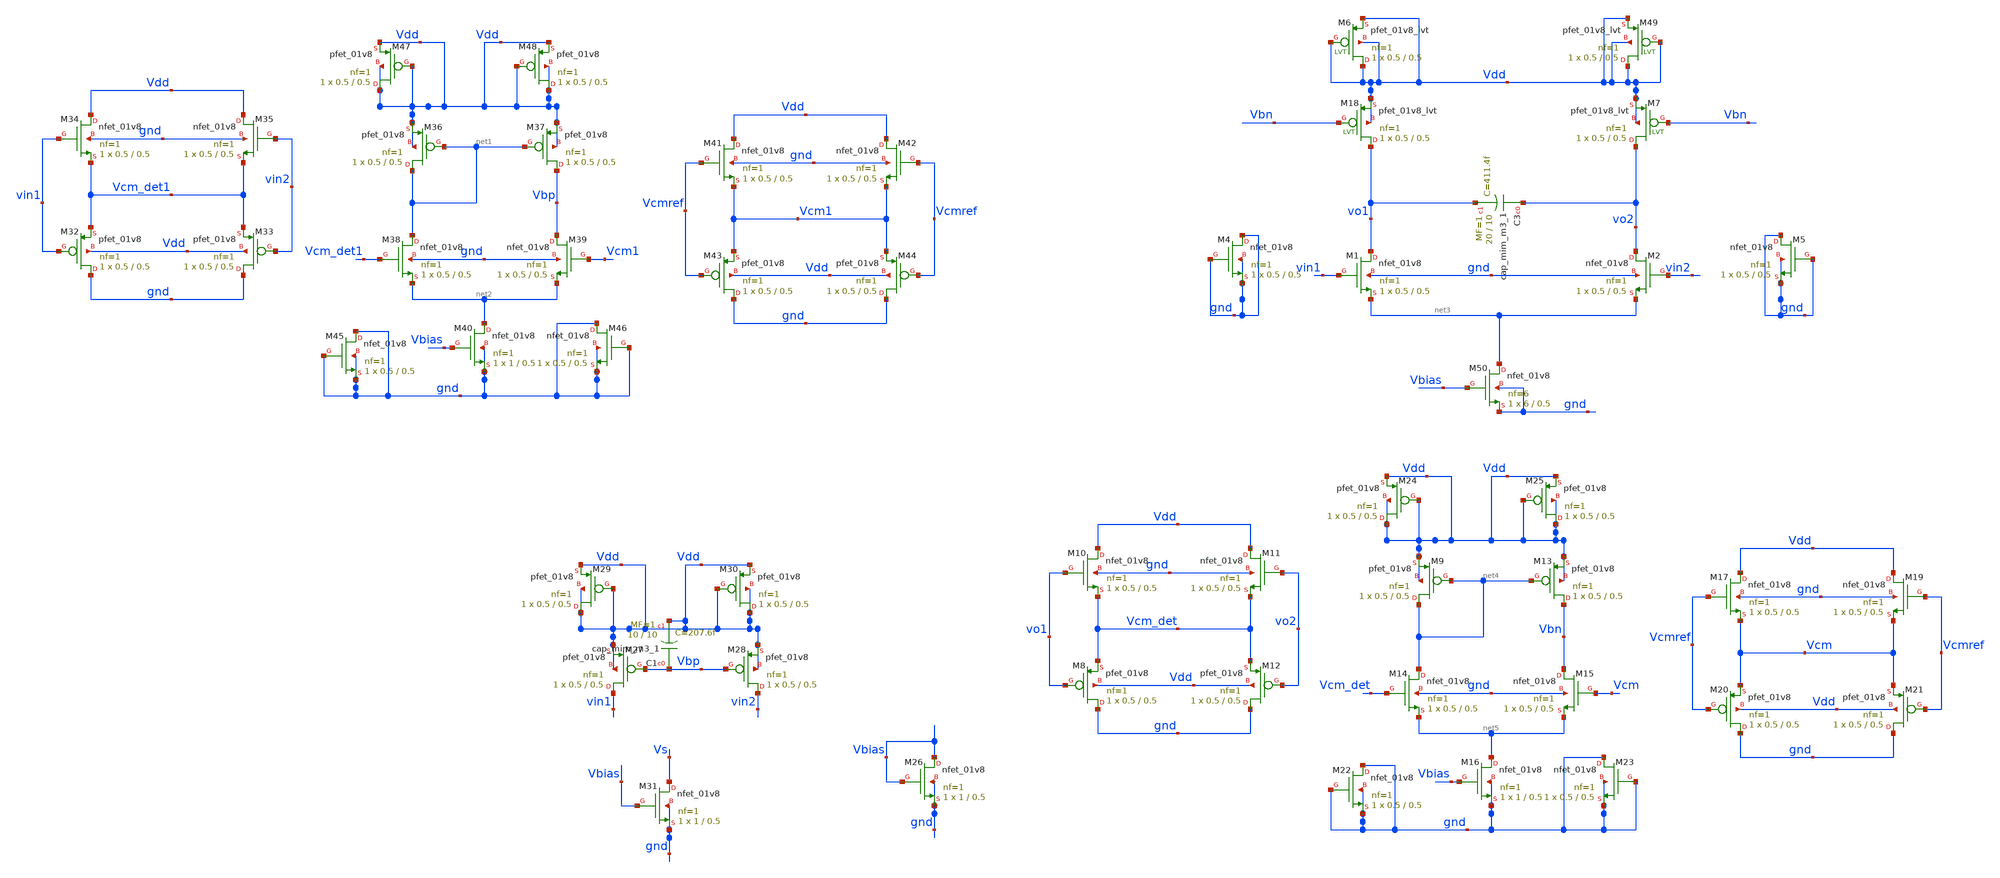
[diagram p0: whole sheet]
** sch_path: xschem/xschemfiles/full_new1.sch
**.subckt full_new1
XM26 Vbias Vbias gnd gnd sky130_fd_pr__nfet_01v8 L=0.5 W=1 nf=1 ad='int((nf+1)/2) * W/nf * 0.29' as='int((nf+2)/2) * W/nf * 0.29'
+ pd='2*int((nf+1)/2) * (W/nf + 0.29)' ps='2*int((nf+2)/2) * (W/nf + 0.29)' nrd='0.29 / W' nrs='0.29 / W'
+ sa=0 sb=0 sd=0 mult=1 m=1
XM27 vin1 Vbp Vdd Vdd sky130_fd_pr__pfet_01v8 L=0.5 W=0.5 nf=1 ad='int((nf+1)/2) * W/nf * 0.29' as='int((nf+2)/2) * W/nf * 0.29'
+ pd='2*int((nf+1)/2) * (W/nf + 0.29)' ps='2*int((nf+2)/2) * (W/nf + 0.29)' nrd='0.29 / W' nrs='0.29 / W'
+ sa=0 sb=0 sd=0 mult=1 m=1
XM28 vin2 Vbp Vdd Vdd sky130_fd_pr__pfet_01v8 L=0.5 W=0.5 nf=1 ad='int((nf+1)/2) * W/nf * 0.29' as='int((nf+2)/2) * W/nf * 0.29'
+ pd='2*int((nf+1)/2) * (W/nf + 0.29)' ps='2*int((nf+2)/2) * (W/nf + 0.29)' nrd='0.29 / W' nrs='0.29 / W'
+ sa=0 sb=0 sd=0 mult=1 m=1
XM29 Vdd Vdd Vdd Vdd sky130_fd_pr__pfet_01v8 L=0.5 W=0.5 nf=1 ad='int((nf+1)/2) * W/nf * 0.29' as='int((nf+2)/2) * W/nf * 0.29'
+ pd='2*int((nf+1)/2) * (W/nf + 0.29)' ps='2*int((nf+2)/2) * (W/nf + 0.29)' nrd='0.29 / W' nrs='0.29 / W'
+ sa=0 sb=0 sd=0 mult=1 m=1
XM30 Vdd Vdd Vdd Vdd sky130_fd_pr__pfet_01v8 L=0.5 W=0.5 nf=1 ad='int((nf+1)/2) * W/nf * 0.29' as='int((nf+2)/2) * W/nf * 0.29'
+ pd='2*int((nf+1)/2) * (W/nf + 0.29)' ps='2*int((nf+2)/2) * (W/nf + 0.29)' nrd='0.29 / W' nrs='0.29 / W'
+ sa=0 sb=0 sd=0 mult=1 m=1
XM31 Vs Vbias gnd gnd sky130_fd_pr__nfet_01v8 L=0.5 W=1 nf=1 ad='int((nf+1)/2) * W/nf * 0.29' as='int((nf+2)/2) * W/nf * 0.29'
+ pd='2*int((nf+1)/2) * (W/nf + 0.29)' ps='2*int((nf+2)/2) * (W/nf + 0.29)' nrd='0.29 / W' nrs='0.29 / W'
+ sa=0 sb=0 sd=0 mult=1 m=1
XC1 Vbp Vdd sky130_fd_pr__cap_mim_m3_1 W=10 L=10 MF=1 m=1
XM32 gnd vin1 Vcm_det1 Vdd sky130_fd_pr__pfet_01v8 L=0.5 W=0.5 nf=1 ad='int((nf+1)/2) * W/nf * 0.29'
+ as='int((nf+2)/2) * W/nf * 0.29' pd='2*int((nf+1)/2) * (W/nf + 0.29)' ps='2*int((nf+2)/2) * (W/nf + 0.29)'
+ nrd='0.29 / W' nrs='0.29 / W' sa=0 sb=0 sd=0 mult=1 m=1
XM33 gnd vin2 Vcm_det1 Vdd sky130_fd_pr__pfet_01v8 L=0.5 W=0.5 nf=1 ad='int((nf+1)/2) * W/nf * 0.29'
+ as='int((nf+2)/2) * W/nf * 0.29' pd='2*int((nf+1)/2) * (W/nf + 0.29)' ps='2*int((nf+2)/2) * (W/nf + 0.29)'
+ nrd='0.29 / W' nrs='0.29 / W' sa=0 sb=0 sd=0 mult=1 m=1
XM34 Vdd vin1 Vcm_det1 gnd sky130_fd_pr__nfet_01v8 L=0.5 W=0.5 nf=1 ad='int((nf+1)/2) * W/nf * 0.29'
+ as='int((nf+2)/2) * W/nf * 0.29' pd='2*int((nf+1)/2) * (W/nf + 0.29)' ps='2*int((nf+2)/2) * (W/nf + 0.29)'
+ nrd='0.29 / W' nrs='0.29 / W' sa=0 sb=0 sd=0 mult=1 m=1
XM35 Vdd vin2 Vcm_det1 gnd sky130_fd_pr__nfet_01v8 L=0.5 W=0.5 nf=1 ad='int((nf+1)/2) * W/nf * 0.29'
+ as='int((nf+2)/2) * W/nf * 0.29' pd='2*int((nf+1)/2) * (W/nf + 0.29)' ps='2*int((nf+2)/2) * (W/nf + 0.29)'
+ nrd='0.29 / W' nrs='0.29 / W' sa=0 sb=0 sd=0 mult=1 m=1
XM36 net1 net1 Vdd Vdd sky130_fd_pr__pfet_01v8 L=0.5 W=0.5 nf=1 ad='int((nf+1)/2) * W/nf * 0.29' as='int((nf+2)/2) * W/nf * 0.29'
+ pd='2*int((nf+1)/2) * (W/nf + 0.29)' ps='2*int((nf+2)/2) * (W/nf + 0.29)' nrd='0.29 / W' nrs='0.29 / W'
+ sa=0 sb=0 sd=0 mult=1 m=1
XM37 Vbp net1 Vdd Vdd sky130_fd_pr__pfet_01v8 L=0.5 W=0.5 nf=1 ad='int((nf+1)/2) * W/nf * 0.29' as='int((nf+2)/2) * W/nf * 0.29'
+ pd='2*int((nf+1)/2) * (W/nf + 0.29)' ps='2*int((nf+2)/2) * (W/nf + 0.29)' nrd='0.29 / W' nrs='0.29 / W'
+ sa=0 sb=0 sd=0 mult=1 m=1
XM38 net1 Vcm_det1 net2 gnd sky130_fd_pr__nfet_01v8 L=0.5 W=0.5 nf=1 ad='int((nf+1)/2) * W/nf * 0.29'
+ as='int((nf+2)/2) * W/nf * 0.29' pd='2*int((nf+1)/2) * (W/nf + 0.29)' ps='2*int((nf+2)/2) * (W/nf + 0.29)'
+ nrd='0.29 / W' nrs='0.29 / W' sa=0 sb=0 sd=0 mult=1 m=1
XM39 Vbp Vcm1 net2 gnd sky130_fd_pr__nfet_01v8 L=0.5 W=0.5 nf=1 ad='int((nf+1)/2) * W/nf * 0.29' as='int((nf+2)/2) * W/nf * 0.29'
+ pd='2*int((nf+1)/2) * (W/nf + 0.29)' ps='2*int((nf+2)/2) * (W/nf + 0.29)' nrd='0.29 / W' nrs='0.29 / W'
+ sa=0 sb=0 sd=0 mult=1 m=1
XM40 net2 Vbias gnd gnd sky130_fd_pr__nfet_01v8 L=0.5 W=1 nf=1 ad='int((nf+1)/2) * W/nf * 0.29' as='int((nf+2)/2) * W/nf * 0.29'
+ pd='2*int((nf+1)/2) * (W/nf + 0.29)' ps='2*int((nf+2)/2) * (W/nf + 0.29)' nrd='0.29 / W' nrs='0.29 / W'
+ sa=0 sb=0 sd=0 mult=1 m=1
XM41 Vdd Vcmref Vcm1 gnd sky130_fd_pr__nfet_01v8 L=0.5 W=0.5 nf=1 ad='int((nf+1)/2) * W/nf * 0.29' as='int((nf+2)/2) * W/nf * 0.29'
+ pd='2*int((nf+1)/2) * (W/nf + 0.29)' ps='2*int((nf+2)/2) * (W/nf + 0.29)' nrd='0.29 / W' nrs='0.29 / W'
+ sa=0 sb=0 sd=0 mult=1 m=1
XM42 Vdd Vcmref Vcm1 gnd sky130_fd_pr__nfet_01v8 L=0.5 W=0.5 nf=1 ad='int((nf+1)/2) * W/nf * 0.29' as='int((nf+2)/2) * W/nf * 0.29'
+ pd='2*int((nf+1)/2) * (W/nf + 0.29)' ps='2*int((nf+2)/2) * (W/nf + 0.29)' nrd='0.29 / W' nrs='0.29 / W'
+ sa=0 sb=0 sd=0 mult=1 m=1
XM43 gnd Vcmref Vcm1 Vdd sky130_fd_pr__pfet_01v8 L=0.5 W=0.5 nf=1 ad='int((nf+1)/2) * W/nf * 0.29' as='int((nf+2)/2) * W/nf * 0.29'
+ pd='2*int((nf+1)/2) * (W/nf + 0.29)' ps='2*int((nf+2)/2) * (W/nf + 0.29)' nrd='0.29 / W' nrs='0.29 / W'
+ sa=0 sb=0 sd=0 mult=1 m=1
XM44 gnd Vcmref Vcm1 Vdd sky130_fd_pr__pfet_01v8 L=0.5 W=0.5 nf=1 ad='int((nf+1)/2) * W/nf * 0.29' as='int((nf+2)/2) * W/nf * 0.29'
+ pd='2*int((nf+1)/2) * (W/nf + 0.29)' ps='2*int((nf+2)/2) * (W/nf + 0.29)' nrd='0.29 / W' nrs='0.29 / W'
+ sa=0 sb=0 sd=0 mult=1 m=1
XM45 gnd gnd gnd gnd sky130_fd_pr__nfet_01v8 L=0.5 W=0.5 nf=1 ad='int((nf+1)/2) * W/nf * 0.29' as='int((nf+2)/2) * W/nf * 0.29'
+ pd='2*int((nf+1)/2) * (W/nf + 0.29)' ps='2*int((nf+2)/2) * (W/nf + 0.29)' nrd='0.29 / W' nrs='0.29 / W'
+ sa=0 sb=0 sd=0 mult=1 m=1
XM46 gnd gnd gnd gnd sky130_fd_pr__nfet_01v8 L=0.5 W=0.5 nf=1 ad='int((nf+1)/2) * W/nf * 0.29' as='int((nf+2)/2) * W/nf * 0.29'
+ pd='2*int((nf+1)/2) * (W/nf + 0.29)' ps='2*int((nf+2)/2) * (W/nf + 0.29)' nrd='0.29 / W' nrs='0.29 / W'
+ sa=0 sb=0 sd=0 mult=1 m=1
XM47 Vdd Vdd Vdd Vdd sky130_fd_pr__pfet_01v8 L=0.5 W=0.5 nf=1 ad='int((nf+1)/2) * W/nf * 0.29' as='int((nf+2)/2) * W/nf * 0.29'
+ pd='2*int((nf+1)/2) * (W/nf + 0.29)' ps='2*int((nf+2)/2) * (W/nf + 0.29)' nrd='0.29 / W' nrs='0.29 / W'
+ sa=0 sb=0 sd=0 mult=1 m=1
XM48 Vdd Vdd Vdd Vdd sky130_fd_pr__pfet_01v8 L=0.5 W=0.5 nf=1 ad='int((nf+1)/2) * W/nf * 0.29' as='int((nf+2)/2) * W/nf * 0.29'
+ pd='2*int((nf+1)/2) * (W/nf + 0.29)' ps='2*int((nf+2)/2) * (W/nf + 0.29)' nrd='0.29 / W' nrs='0.29 / W'
+ sa=0 sb=0 sd=0 mult=1 m=1
XM1 vo1 vin1 net3 gnd sky130_fd_pr__nfet_01v8 L=0.5 W=0.5 nf=1 ad='int((nf+1)/2) * W/nf * 0.29' as='int((nf+2)/2) * W/nf * 0.29'
+ pd='2*int((nf+1)/2) * (W/nf + 0.29)' ps='2*int((nf+2)/2) * (W/nf + 0.29)' nrd='0.29 / W' nrs='0.29 / W'
+ sa=0 sb=0 sd=0 mult=1 m=1
XM2 vo2 vin2 net3 gnd sky130_fd_pr__nfet_01v8 L=0.5 W=0.5 nf=1 ad='int((nf+1)/2) * W/nf * 0.29' as='int((nf+2)/2) * W/nf * 0.29'
+ pd='2*int((nf+1)/2) * (W/nf + 0.29)' ps='2*int((nf+2)/2) * (W/nf + 0.29)' nrd='0.29 / W' nrs='0.29 / W'
+ sa=0 sb=0 sd=0 mult=1 m=1
XC3 vo2 vo1 sky130_fd_pr__cap_mim_m3_1 W=20 L=10 MF=1 m=1
XM4 gnd gnd gnd gnd sky130_fd_pr__nfet_01v8 L=0.5 W=0.5 nf=1 ad='int((nf+1)/2) * W/nf * 0.29' as='int((nf+2)/2) * W/nf * 0.29'
+ pd='2*int((nf+1)/2) * (W/nf + 0.29)' ps='2*int((nf+2)/2) * (W/nf + 0.29)' nrd='0.29 / W' nrs='0.29 / W'
+ sa=0 sb=0 sd=0 mult=1 m=1
XM5 gnd gnd gnd gnd sky130_fd_pr__nfet_01v8 L=0.5 W=0.5 nf=1 ad='int((nf+1)/2) * W/nf * 0.29' as='int((nf+2)/2) * W/nf * 0.29'
+ pd='2*int((nf+1)/2) * (W/nf + 0.29)' ps='2*int((nf+2)/2) * (W/nf + 0.29)' nrd='0.29 / W' nrs='0.29 / W'
+ sa=0 sb=0 sd=0 mult=1 m=1
XM8 gnd vo1 Vcm_det Vdd sky130_fd_pr__pfet_01v8 L=0.5 W=0.5 nf=1 ad='int((nf+1)/2) * W/nf * 0.29' as='int((nf+2)/2) * W/nf * 0.29'
+ pd='2*int((nf+1)/2) * (W/nf + 0.29)' ps='2*int((nf+2)/2) * (W/nf + 0.29)' nrd='0.29 / W' nrs='0.29 / W'
+ sa=0 sb=0 sd=0 mult=1 m=1
XM12 gnd vo2 Vcm_det Vdd sky130_fd_pr__pfet_01v8 L=0.5 W=0.5 nf=1 ad='int((nf+1)/2) * W/nf * 0.29' as='int((nf+2)/2) * W/nf * 0.29'
+ pd='2*int((nf+1)/2) * (W/nf + 0.29)' ps='2*int((nf+2)/2) * (W/nf + 0.29)' nrd='0.29 / W' nrs='0.29 / W'
+ sa=0 sb=0 sd=0 mult=1 m=1
XM10 Vdd vo1 Vcm_det gnd sky130_fd_pr__nfet_01v8 L=0.5 W=0.5 nf=1 ad='int((nf+1)/2) * W/nf * 0.29' as='int((nf+2)/2) * W/nf * 0.29'
+ pd='2*int((nf+1)/2) * (W/nf + 0.29)' ps='2*int((nf+2)/2) * (W/nf + 0.29)' nrd='0.29 / W' nrs='0.29 / W'
+ sa=0 sb=0 sd=0 mult=1 m=1
XM11 Vdd vo2 Vcm_det gnd sky130_fd_pr__nfet_01v8 L=0.5 W=0.5 nf=1 ad='int((nf+1)/2) * W/nf * 0.29' as='int((nf+2)/2) * W/nf * 0.29'
+ pd='2*int((nf+1)/2) * (W/nf + 0.29)' ps='2*int((nf+2)/2) * (W/nf + 0.29)' nrd='0.29 / W' nrs='0.29 / W'
+ sa=0 sb=0 sd=0 mult=1 m=1
XM9 net4 net4 Vdd Vdd sky130_fd_pr__pfet_01v8 L=0.5 W=0.5 nf=1 ad='int((nf+1)/2) * W/nf * 0.29' as='int((nf+2)/2) * W/nf * 0.29'
+ pd='2*int((nf+1)/2) * (W/nf + 0.29)' ps='2*int((nf+2)/2) * (W/nf + 0.29)' nrd='0.29 / W' nrs='0.29 / W'
+ sa=0 sb=0 sd=0 mult=1 m=1
XM13 Vbn net4 Vdd Vdd sky130_fd_pr__pfet_01v8 L=0.5 W=0.5 nf=1 ad='int((nf+1)/2) * W/nf * 0.29' as='int((nf+2)/2) * W/nf * 0.29'
+ pd='2*int((nf+1)/2) * (W/nf + 0.29)' ps='2*int((nf+2)/2) * (W/nf + 0.29)' nrd='0.29 / W' nrs='0.29 / W'
+ sa=0 sb=0 sd=0 mult=1 m=1
XM14 net4 Vcm_det net5 gnd sky130_fd_pr__nfet_01v8 L=0.5 W=0.5 nf=1 ad='int((nf+1)/2) * W/nf * 0.29'
+ as='int((nf+2)/2) * W/nf * 0.29' pd='2*int((nf+1)/2) * (W/nf + 0.29)' ps='2*int((nf+2)/2) * (W/nf + 0.29)'
+ nrd='0.29 / W' nrs='0.29 / W' sa=0 sb=0 sd=0 mult=1 m=1
XM15 Vbn Vcm net5 gnd sky130_fd_pr__nfet_01v8 L=0.5 W=0.5 nf=1 ad='int((nf+1)/2) * W/nf * 0.29' as='int((nf+2)/2) * W/nf * 0.29'
+ pd='2*int((nf+1)/2) * (W/nf + 0.29)' ps='2*int((nf+2)/2) * (W/nf + 0.29)' nrd='0.29 / W' nrs='0.29 / W'
+ sa=0 sb=0 sd=0 mult=1 m=1
XM16 net5 Vbias gnd gnd sky130_fd_pr__nfet_01v8 L=0.5 W=1 nf=1 ad='int((nf+1)/2) * W/nf * 0.29' as='int((nf+2)/2) * W/nf * 0.29'
+ pd='2*int((nf+1)/2) * (W/nf + 0.29)' ps='2*int((nf+2)/2) * (W/nf + 0.29)' nrd='0.29 / W' nrs='0.29 / W'
+ sa=0 sb=0 sd=0 mult=1 m=1
XM17 Vdd Vcmref Vcm gnd sky130_fd_pr__nfet_01v8 L=0.5 W=0.5 nf=1 ad='int((nf+1)/2) * W/nf * 0.29' as='int((nf+2)/2) * W/nf * 0.29'
+ pd='2*int((nf+1)/2) * (W/nf + 0.29)' ps='2*int((nf+2)/2) * (W/nf + 0.29)' nrd='0.29 / W' nrs='0.29 / W'
+ sa=0 sb=0 sd=0 mult=1 m=1
XM19 Vdd Vcmref Vcm gnd sky130_fd_pr__nfet_01v8 L=0.5 W=0.5 nf=1 ad='int((nf+1)/2) * W/nf * 0.29' as='int((nf+2)/2) * W/nf * 0.29'
+ pd='2*int((nf+1)/2) * (W/nf + 0.29)' ps='2*int((nf+2)/2) * (W/nf + 0.29)' nrd='0.29 / W' nrs='0.29 / W'
+ sa=0 sb=0 sd=0 mult=1 m=1
XM20 gnd Vcmref Vcm Vdd sky130_fd_pr__pfet_01v8 L=0.5 W=0.5 nf=1 ad='int((nf+1)/2) * W/nf * 0.29' as='int((nf+2)/2) * W/nf * 0.29'
+ pd='2*int((nf+1)/2) * (W/nf + 0.29)' ps='2*int((nf+2)/2) * (W/nf + 0.29)' nrd='0.29 / W' nrs='0.29 / W'
+ sa=0 sb=0 sd=0 mult=1 m=1
XM21 gnd Vcmref Vcm Vdd sky130_fd_pr__pfet_01v8 L=0.5 W=0.5 nf=1 ad='int((nf+1)/2) * W/nf * 0.29' as='int((nf+2)/2) * W/nf * 0.29'
+ pd='2*int((nf+1)/2) * (W/nf + 0.29)' ps='2*int((nf+2)/2) * (W/nf + 0.29)' nrd='0.29 / W' nrs='0.29 / W'
+ sa=0 sb=0 sd=0 mult=1 m=1
XM22 gnd gnd gnd gnd sky130_fd_pr__nfet_01v8 L=0.5 W=0.5 nf=1 ad='int((nf+1)/2) * W/nf * 0.29' as='int((nf+2)/2) * W/nf * 0.29'
+ pd='2*int((nf+1)/2) * (W/nf + 0.29)' ps='2*int((nf+2)/2) * (W/nf + 0.29)' nrd='0.29 / W' nrs='0.29 / W'
+ sa=0 sb=0 sd=0 mult=1 m=1
XM23 gnd gnd gnd gnd sky130_fd_pr__nfet_01v8 L=0.5 W=0.5 nf=1 ad='int((nf+1)/2) * W/nf * 0.29' as='int((nf+2)/2) * W/nf * 0.29'
+ pd='2*int((nf+1)/2) * (W/nf + 0.29)' ps='2*int((nf+2)/2) * (W/nf + 0.29)' nrd='0.29 / W' nrs='0.29 / W'
+ sa=0 sb=0 sd=0 mult=1 m=1
XM24 Vdd Vdd Vdd Vdd sky130_fd_pr__pfet_01v8 L=0.5 W=0.5 nf=1 ad='int((nf+1)/2) * W/nf * 0.29' as='int((nf+2)/2) * W/nf * 0.29'
+ pd='2*int((nf+1)/2) * (W/nf + 0.29)' ps='2*int((nf+2)/2) * (W/nf + 0.29)' nrd='0.29 / W' nrs='0.29 / W'
+ sa=0 sb=0 sd=0 mult=1 m=1
XM25 Vdd Vdd Vdd Vdd sky130_fd_pr__pfet_01v8 L=0.5 W=0.5 nf=1 ad='int((nf+1)/2) * W/nf * 0.29' as='int((nf+2)/2) * W/nf * 0.29'
+ pd='2*int((nf+1)/2) * (W/nf + 0.29)' ps='2*int((nf+2)/2) * (W/nf + 0.29)' nrd='0.29 / W' nrs='0.29 / W'
+ sa=0 sb=0 sd=0 mult=1 m=1
XM18 vo1 Vbn Vdd Vdd sky130_fd_pr__pfet_01v8_lvt L=0.5 W=0.5 nf=1 ad='int((nf+1)/2) * W/nf * 0.29' as='int((nf+2)/2) * W/nf * 0.29'
+ pd='2*int((nf+1)/2) * (W/nf + 0.29)' ps='2*int((nf+2)/2) * (W/nf + 0.29)' nrd='0.29 / W' nrs='0.29 / W'
+ sa=0 sb=0 sd=0 mult=1 m=1
XM6 Vdd Vdd Vdd Vdd sky130_fd_pr__pfet_01v8_lvt L=0.5 W=0.5 nf=1 ad='int((nf+1)/2) * W/nf * 0.29' as='int((nf+2)/2) * W/nf * 0.29'
+ pd='2*int((nf+1)/2) * (W/nf + 0.29)' ps='2*int((nf+2)/2) * (W/nf + 0.29)' nrd='0.29 / W' nrs='0.29 / W'
+ sa=0 sb=0 sd=0 mult=1 m=1
XM7 vo2 Vbn Vdd Vdd sky130_fd_pr__pfet_01v8_lvt L=0.5 W=0.5 nf=1 ad='int((nf+1)/2) * W/nf * 0.29' as='int((nf+2)/2) * W/nf * 0.29'
+ pd='2*int((nf+1)/2) * (W/nf + 0.29)' ps='2*int((nf+2)/2) * (W/nf + 0.29)' nrd='0.29 / W' nrs='0.29 / W'
+ sa=0 sb=0 sd=0 mult=1 m=1
XM49 Vdd Vdd Vdd Vdd sky130_fd_pr__pfet_01v8_lvt L=0.5 W=0.5 nf=1 ad='int((nf+1)/2) * W/nf * 0.29' as='int((nf+2)/2) * W/nf * 0.29'
+ pd='2*int((nf+1)/2) * (W/nf + 0.29)' ps='2*int((nf+2)/2) * (W/nf + 0.29)' nrd='0.29 / W' nrs='0.29 / W'
+ sa=0 sb=0 sd=0 mult=1 m=1
XM50 net3 Vbias gnd gnd sky130_fd_pr__nfet_01v8 L=0.5 W=6 nf=6 ad='int((nf+1)/2) * W/nf * 0.29' as='int((nf+2)/2) * W/nf * 0.29'
+ pd='2*int((nf+1)/2) * (W/nf + 0.29)' ps='2*int((nf+2)/2) * (W/nf + 0.29)' nrd='0.29 / W' nrs='0.29 / W'
+ sa=0 sb=0 sd=0 mult=1 m=1
**.ends
.end
